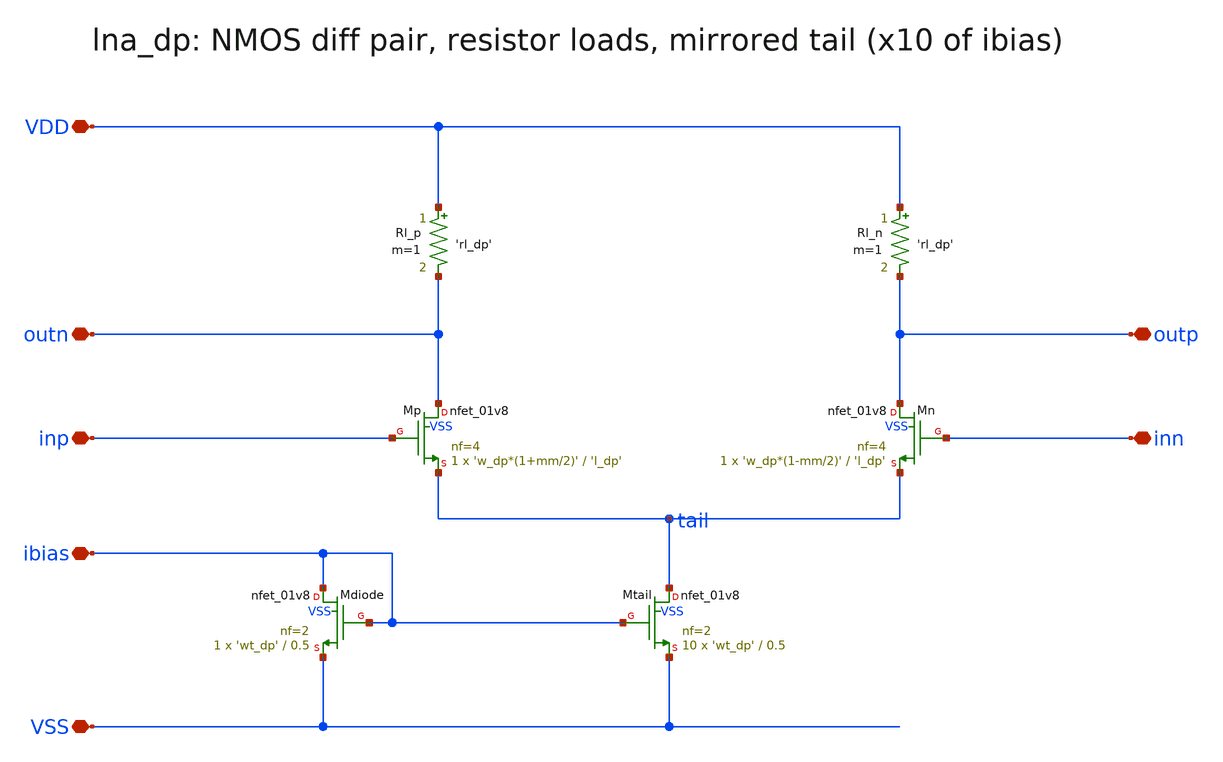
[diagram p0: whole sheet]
** sch_path: xschem/lna_dp.sch
**.subckt lna_dp VDD VSS ibias inp inn outp outn
*.iopin VDD
*.iopin VSS
*.iopin ibias
*.iopin inp
*.iopin inn
*.iopin outp
*.iopin outn
Rl_p VDD outn 'rl_dp' m=1
XMp outn inp tail VSS sky130_fd_pr__nfet_01v8 L='l_dp' W='w_dp*(1+mm/2)' nf=4 ad='int((nf+1)/2) * W/nf * 0.29'
+ as='int((nf+2)/2) * W/nf * 0.29' pd='2*int((nf+1)/2) * (W/nf + 0.29)' ps='2*int((nf+2)/2) * (W/nf + 0.29)'
+ nrd='0.29 / W' nrs='0.29 / W' sa=0 sb=0 sd=0 mult=1 m=1
Rl_n VDD outp 'rl_dp' m=1
XMn outp inn tail VSS sky130_fd_pr__nfet_01v8 L='l_dp' W='w_dp*(1-mm/2)' nf=4 ad='int((nf+1)/2) * W/nf * 0.29'
+ as='int((nf+2)/2) * W/nf * 0.29' pd='2*int((nf+1)/2) * (W/nf + 0.29)' ps='2*int((nf+2)/2) * (W/nf + 0.29)'
+ nrd='0.29 / W' nrs='0.29 / W' sa=0 sb=0 sd=0 mult=1 m=1
XMtail tail ibias VSS VSS sky130_fd_pr__nfet_01v8 L=0.5 W='wt_dp' nf=2 ad='int((nf+1)/2) * W/nf * 0.29'
+ as='int((nf+2)/2) * W/nf * 0.29' pd='2*int((nf+1)/2) * (W/nf + 0.29)' ps='2*int((nf+2)/2) * (W/nf + 0.29)'
+ nrd='0.29 / W' nrs='0.29 / W' sa=0 sb=0 sd=0 mult=10 m=10
XMdiode ibias ibias VSS VSS sky130_fd_pr__nfet_01v8 L=0.5 W='wt_dp' nf=2 ad='int((nf+1)/2) * W/nf * 0.29'
+ as='int((nf+2)/2) * W/nf * 0.29' pd='2*int((nf+1)/2) * (W/nf + 0.29)' ps='2*int((nf+2)/2) * (W/nf + 0.29)'
+ nrd='0.29 / W' nrs='0.29 / W' sa=0 sb=0 sd=0 mult=1 m=1
**.ends
.end
